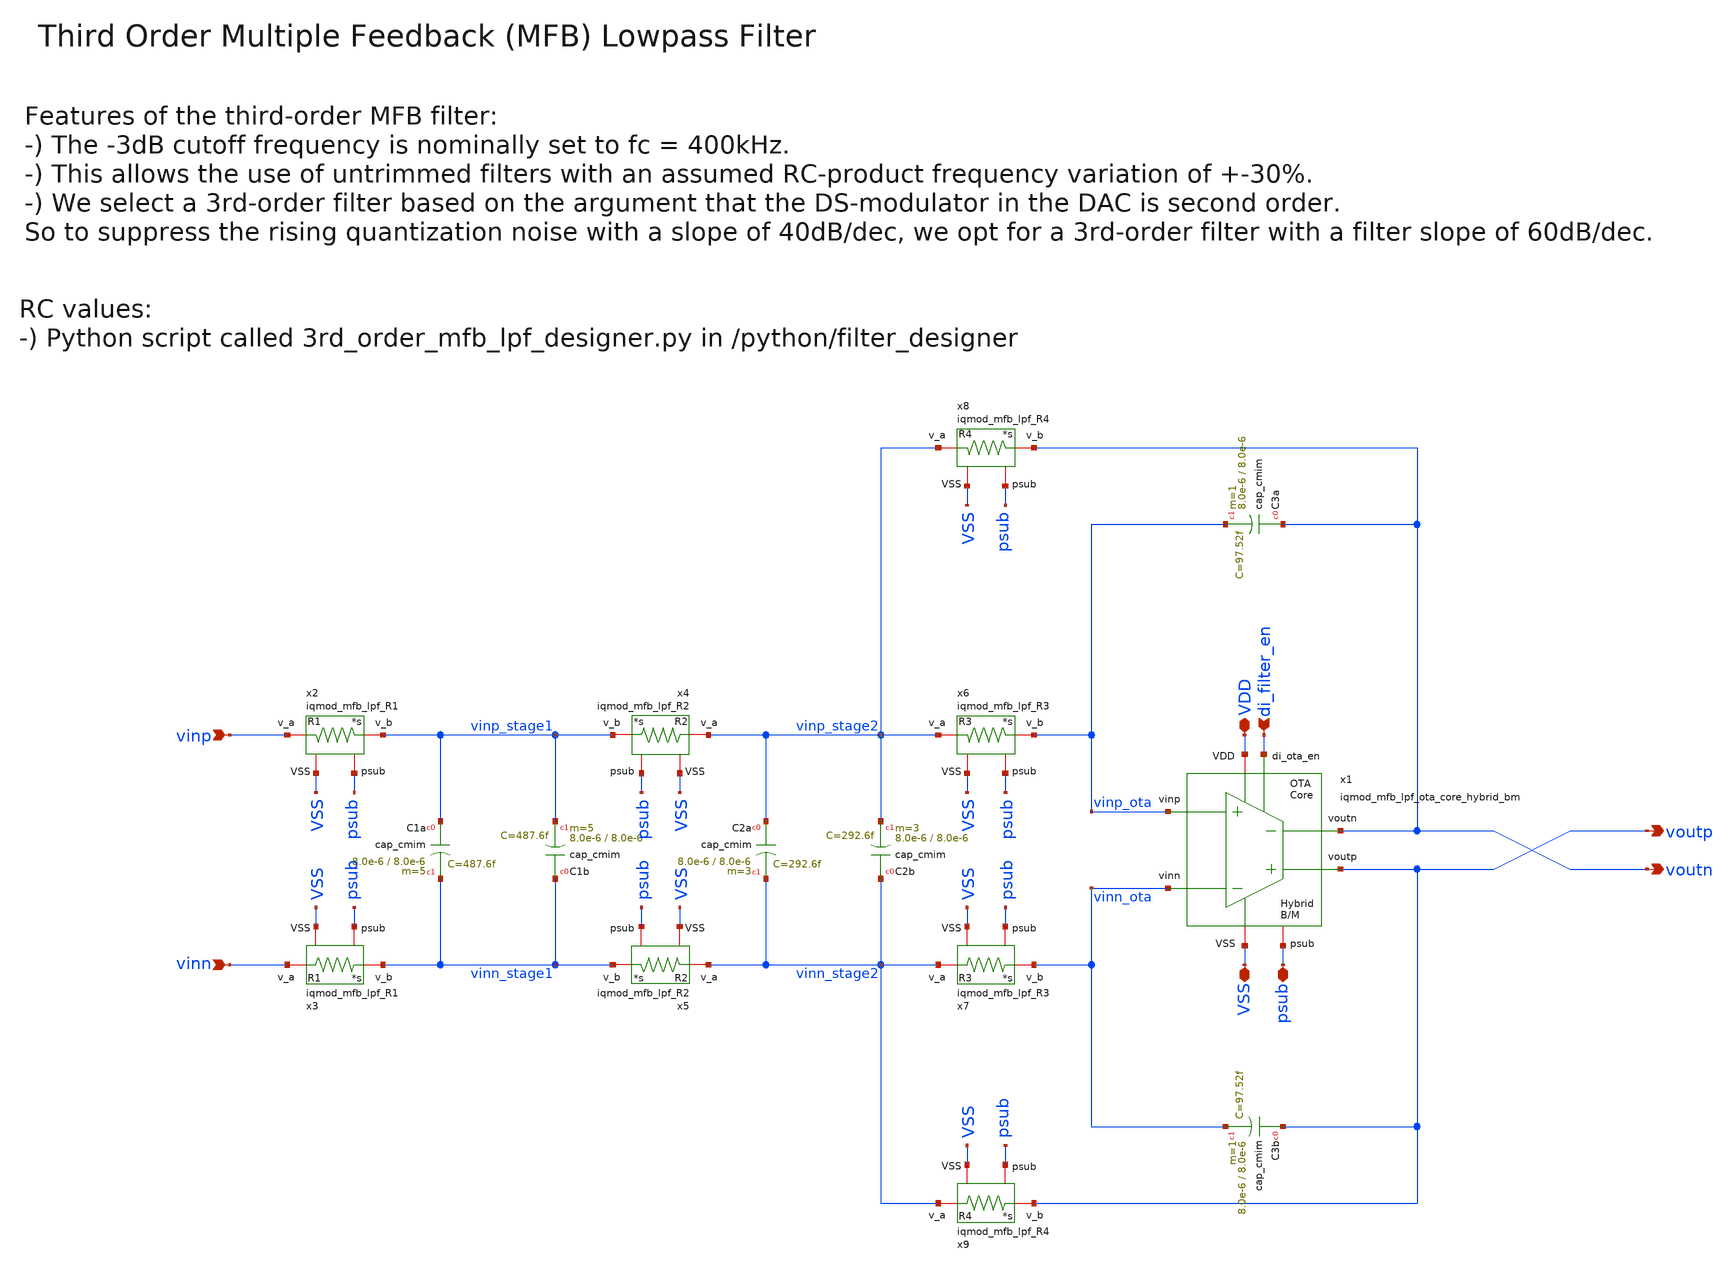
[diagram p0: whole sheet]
** sch_path: ihp130/macros/iqmod/xschem/iqmod_mfb_lpf.sch
**.subckt iqmod_mfb_lpf VDD VSS vinp vinn voutp voutn di_filter_en psub
*.iopin VDD
*.iopin VSS
*.ipin vinp
*.ipin vinn
*.opin voutp
*.opin voutn
*.ipin di_filter_en
*.iopin psub
x1 psub voutp voutn vinn_ota vinp_ota VDD VSS di_filter_en iqmod_mfb_lpf_ota_core_hybrid_bm
XC1a vinp_stage1 vinn_stage1 cap_cmim w=8.0e-6 l=8.0e-6 m=5 mm_ok=1
XC1b vinn_stage1 vinp_stage1 cap_cmim w=8.0e-6 l=8.0e-6 m=5 mm_ok=1
XC2a vinp_stage2 vinn_stage2 cap_cmim w=8.0e-6 l=8.0e-6 m=3 mm_ok=1
XC2b vinn_stage2 vinp_stage2 cap_cmim w=8.0e-6 l=8.0e-6 m=3 mm_ok=1
XC3a voutn vinp_ota cap_cmim w=8.0e-6 l=8.0e-6 m=1 mm_ok=1
XC3b voutp vinn_ota cap_cmim w=8.0e-6 l=8.0e-6 m=1 mm_ok=1
x2 psub vinp_stage1 vinp VSS iqmod_mfb_lpf_R1
x3 psub vinn_stage1 vinn VSS iqmod_mfb_lpf_R1
x4 vinp_stage1 vinp_stage2 psub VSS iqmod_mfb_lpf_R2
x5 vinn_stage1 vinn_stage2 psub VSS iqmod_mfb_lpf_R2
x6 vinp_ota vinp_stage2 psub VSS iqmod_mfb_lpf_R3
x7 vinn_ota vinn_stage2 psub VSS iqmod_mfb_lpf_R3
x8 voutn vinp_stage2 psub VSS iqmod_mfb_lpf_R4
x9 voutp vinn_stage2 psub VSS iqmod_mfb_lpf_R4
**.ends
.end
